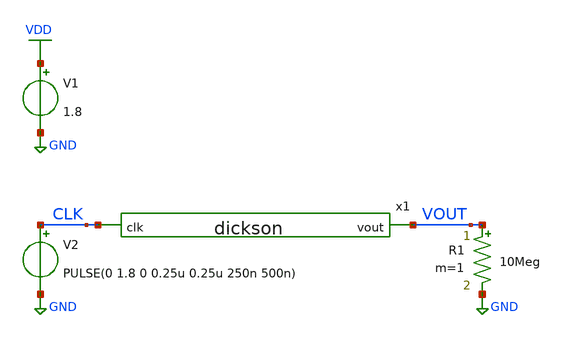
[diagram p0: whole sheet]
** sch_path: xschem/testbench.sch
**.subckt testbench
x1 VOUT CLK dickson
R1 VOUT GND 10Meg m=1
V1 VDD GND 1.8
V2 CLK GND PULSE(0 1.8 0 0.25u 0.25u 250n 500n)
**** begin user architecture code

** opencircuitdesign pdks install
.lib $::SKYWATER_MODELS/sky130.lib.spice tt





.tran 10n 100u
.save all

.control
run
write testbench.raw
.endc


**** end user architecture code
**.ends

* expanding   symbol:  dickson.sym # of pins=2
** sym_path: xschem/dickson.sym
** sch_path: xschem/dickson.sch
.subckt dickson vout clk
*.ipin clk
*.opin vout
XM1 clka clk VDD VDD sky130_fd_pr__pfet_01v8 L=0.15 W=1.5 nf=1 ad='int((nf+1)/2) * W/nf * 0.29' as='int((nf+2)/2) * W/nf * 0.29'
+ pd='2*int((nf+1)/2) * (W/nf + 0.29)' ps='2*int((nf+2)/2) * (W/nf + 0.29)' nrd='0.29 / W' nrs='0.29 / W'
+ sa=0 sb=0 sd=0 mult=1 m=1
XM3 clka clk GND GND sky130_fd_pr__nfet_01v8 L=0.15 W=1 nf=1 ad='int((nf+1)/2) * W/nf * 0.29' as='int((nf+2)/2) * W/nf * 0.29'
+ pd='2*int((nf+1)/2) * (W/nf + 0.29)' ps='2*int((nf+2)/2) * (W/nf + 0.29)' nrd='0.29 / W' nrs='0.29 / W'
+ sa=0 sb=0 sd=0 mult=1 m=1
XM2 clkb clka VDD VDD sky130_fd_pr__pfet_01v8 L=0.15 W=1.5 nf=1 ad='int((nf+1)/2) * W/nf * 0.29' as='int((nf+2)/2) * W/nf * 0.29'
+ pd='2*int((nf+1)/2) * (W/nf + 0.29)' ps='2*int((nf+2)/2) * (W/nf + 0.29)' nrd='0.29 / W' nrs='0.29 / W'
+ sa=0 sb=0 sd=0 mult=1 m=1
XM4 clkb clka GND GND sky130_fd_pr__nfet_01v8 L=0.15 W=1 nf=1 ad='int((nf+1)/2) * W/nf * 0.29' as='int((nf+2)/2) * W/nf * 0.29'
+ pd='2*int((nf+1)/2) * (W/nf + 0.29)' ps='2*int((nf+2)/2) * (W/nf + 0.29)' nrd='0.29 / W' nrs='0.29 / W'
+ sa=0 sb=0 sd=0 mult=1 m=1
XC3 clka stage3 sky130_fd_pr__cap_mim_m3_1 W=50 L=100 MF=1 m=1
XM5 stage1 VDD VDD VDD sky130_fd_pr__nfet_01v8_lvt L=8 W=7 nf=1 ad='int((nf+1)/2) * W/nf * 0.29' as='int((nf+2)/2) * W/nf * 0.29'
+ pd='2*int((nf+1)/2) * (W/nf + 0.29)' ps='2*int((nf+2)/2) * (W/nf + 0.29)' nrd='0.29 / W' nrs='0.29 / W'
+ sa=0 sb=0 sd=0 mult=1 m=1
XC1 clka stage1 sky130_fd_pr__cap_mim_m3_1 W=50 L=100 MF=1 m=1
XM6 stage2 stage1 stage1 stage1 sky130_fd_pr__nfet_01v8_lvt L=8 W=7 nf=1 ad='int((nf+1)/2) * W/nf * 0.29'
+ as='int((nf+2)/2) * W/nf * 0.29' pd='2*int((nf+1)/2) * (W/nf + 0.29)' ps='2*int((nf+2)/2) * (W/nf + 0.29)'
+ nrd='0.29 / W' nrs='0.29 / W' sa=0 sb=0 sd=0 mult=1 m=1
XM7 stage3 stage2 stage2 stage2 sky130_fd_pr__nfet_01v8_lvt L=8 W=7 nf=1 ad='int((nf+1)/2) * W/nf * 0.29'
+ as='int((nf+2)/2) * W/nf * 0.29' pd='2*int((nf+1)/2) * (W/nf + 0.29)' ps='2*int((nf+2)/2) * (W/nf + 0.29)'
+ nrd='0.29 / W' nrs='0.29 / W' sa=0 sb=0 sd=0 mult=1 m=1
XC2 clkb stage2 sky130_fd_pr__cap_mim_m3_1 W=50 L=100 MF=1 m=1
XM8 vout stage3 stage3 stage3 sky130_fd_pr__nfet_01v8_lvt L=8 W=7 nf=1 ad='int((nf+1)/2) * W/nf * 0.29'
+ as='int((nf+2)/2) * W/nf * 0.29' pd='2*int((nf+1)/2) * (W/nf + 0.29)' ps='2*int((nf+2)/2) * (W/nf + 0.29)'
+ nrd='0.29 / W' nrs='0.29 / W' sa=0 sb=0 sd=0 mult=1 m=1
XC4 GND vout sky130_fd_pr__cap_mim_m3_1 W=100 L=100 MF=1 m=1
.ends

.GLOBAL GND
.GLOBAL VDD
.end
